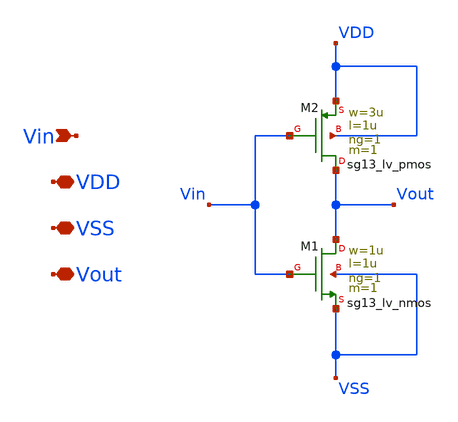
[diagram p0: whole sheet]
** sch_path: Modulo_Analogico/Lab2/inverter.sch
**.subckt inverter Vin VDD VSS Vout
*.ipin Vin
*.iopin VDD
*.iopin VSS
*.iopin Vout
XM1 Vout Vin VSS VSS sg13_lv_nmos w=1u l=1u ng=1 m=1 mm_ok=1
XM2 Vout Vin VDD VDD sg13_lv_pmos w=3u l=1u ng=1 m=1 mm_ok=1
**.ends
.end
